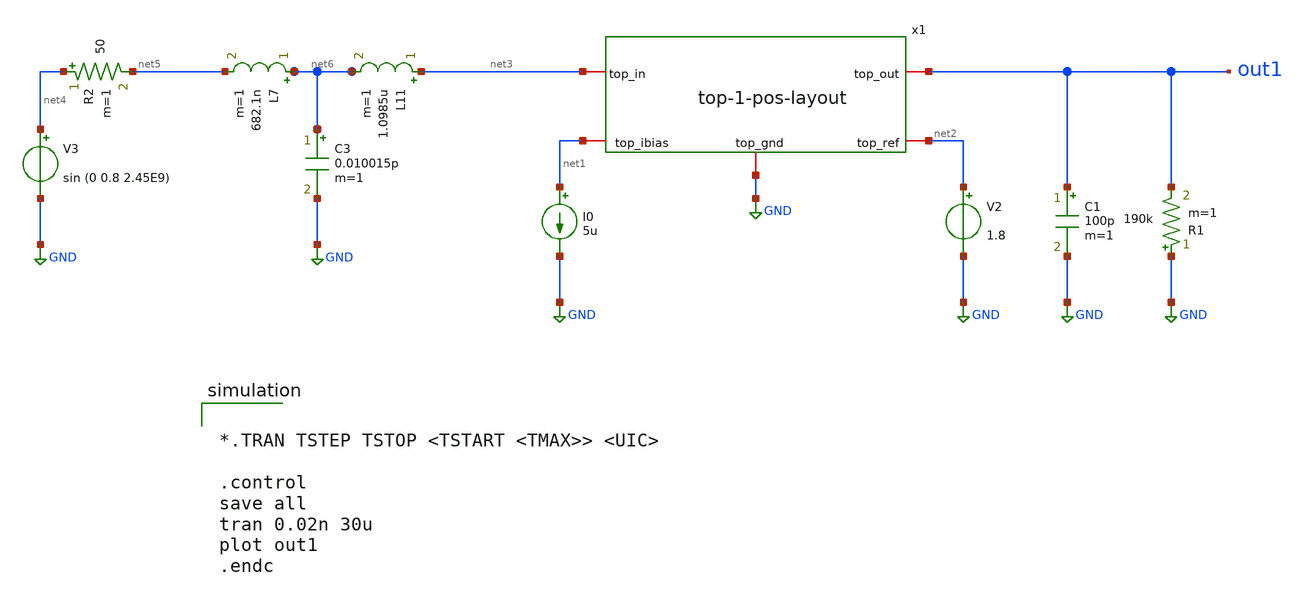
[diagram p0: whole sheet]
** sch_path: xschem/tb-top-1-pos-layout.sch
**.subckt tb-top-1-pos-layout
I0 net1 GND 5u
V2 net2 GND 1.8
C1 out1 GND 100p m=1
R1 GND out1 190k m=1
x1 net3 out1 net2 net1 GND top-1-pos-layout
V3 net4 GND sin (0 0.8 2.45E9)
R2 net4 net5 50 m=1
L7 net6 net5 682.1n m=1
C3 net6 GND 0.010015p m=1
L11 net3 net6 1.0985u m=1
**** begin user architecture code


*.TRAN TSTEP TSTOP <TSTART <TMAX>> <UIC>

.control
save all
tran 0.02n 30u
plot out1
.endc



** opencircuitdesign pdks install
.lib $::SKYWATER_MODELS/sky130.lib.spice tt


**** end user architecture code
**.ends

* expanding   symbol:  top-1-pos-layout.sym # of pins=5
** sym_path: xschem/top-1-pos-layout.sym
** sch_path: xschem/top-1-pos-layout.sch
.subckt top-1-pos-layout top_in top_out top_ref top_ibias top_gnd
*.iopin top_in
*.iopin top_gnd
*.iopin top_ibias
*.iopin top_ref
*.iopin top_out
**** begin user architecture code

* NGSPICE file created from top-1.ext - technology: sky130A

*.subckt top-1 top_ibias top_ref top_out top_in top_gnd
X0 w_13300_10340# top_ibias x1.o x1.o sky130_fd_pr__pfet_g5v0d10v5 ad=5.51e+12p pd=4.206e+07u
+ as=1.392e+13p ps=1.0528e+08u w=3e+06u l=1e+06u
X1 a_11070_13062# x2.x1.Vout sky130_fd_pr__cap_mim_m3_1 l=2.3e+07u w=2.3e+07u
X2 x1.o top_ibias x2.x1.Vout x1.o sky130_fd_pr__pfet_g5v0d10v5 ad=0p pd=0u as=6.09e+12p
+ ps=4.606e+07u w=3e+06u l=1e+06u
X3 x1.o top_ibias w_13300_10340# x1.o sky130_fd_pr__pfet_g5v0d10v5 ad=0p pd=0u as=0p ps=0u w=3e+06u
+ l=1e+06u
X4 x1.o top_ibias w_13300_10340# x1.o sky130_fd_pr__pfet_g5v0d10v5 ad=0p pd=0u as=0p ps=0u w=3e+06u
+ l=1e+06u
X5 top_ibias top_ibias x1.o x1.o sky130_fd_pr__pfet_g5v0d10v5 ad=3.48e+12p pd=2.632e+07u as=0p ps=0u
+ w=3e+06u l=1e+06u
X6 top_out x2.x1.Vout x1.o top_gnd sky130_fd_pr__nfet_03v3_nvt ad=2.9e+12p pd=2.058e+07u
+ as=3.56642e+13p ps=2.4654e+08u w=1e+07u l=500000u
X7 x2.x1.Vout top_ibias x1.o x1.o sky130_fd_pr__pfet_g5v0d10v5 ad=0p pd=0u as=0p ps=0u w=3e+06u
+ l=1e+06u
X8 x2.x1.Vout top_ibias x1.o x1.o sky130_fd_pr__pfet_g5v0d10v5 ad=0p pd=0u as=0p ps=0u w=3e+06u
+ l=1e+06u
X9 w_13300_10340# top_ibias x1.o x1.o sky130_fd_pr__pfet_g5v0d10v5 ad=0p pd=0u as=0p ps=0u w=3e+06u
+ l=1e+06u
X10 x1.o top_ibias top_ibias x1.o sky130_fd_pr__pfet_g5v0d10v5 ad=0p pd=0u as=0p ps=0u w=3e+06u
+ l=1e+06u
X11 x2.x1.Vout top_ibias x1.o x1.o sky130_fd_pr__pfet_g5v0d10v5 ad=0p pd=0u as=0p ps=0u w=3e+06u
+ l=1e+06u
X12 x2.x1.Vout a_11070_13062# top_gnd top_gnd sky130_fd_pr__nfet_g5v0d10v5 ad=3.48e+12p
+ pd=2.632e+07u as=7.54e+12p ps=5.548e+07u w=3e+06u l=1e+06u
X13 x1.o top_ibias x2.x1.Vout x1.o sky130_fd_pr__pfet_g5v0d10v5 ad=0p pd=0u as=0p ps=0u w=3e+06u
+ l=1e+06u
X14 a_11070_13062# top_ref w_13300_10340# w_13300_10340# sky130_fd_pr__pfet_g5v0d10v5 ad=5.8e+11p
+ pd=4.58e+06u as=0p ps=0u w=2e+06u l=500000u
X15 x1.o top_gnd sky130_fd_pr__cap_mim_m3_1 l=3e+07u w=3e+07u
X16 w_100_16400# w_100_16400# top_gnd w_100_16400# sky130_fd_pr__pfet_01v8_lvt ad=1.392e+13p
+ pd=9.948e+07u as=6.96e+12p ps=4.974e+07u w=8e+06u l=350000u
X17 x1.o top_gnd sky130_fd_pr__cap_mim_m3_1 l=3e+07u w=3e+07u
X18 x2.x1.Vout a_11070_13062# top_gnd top_gnd sky130_fd_pr__nfet_g5v0d10v5 ad=0p pd=0u as=0p ps=0u
+ w=3e+06u l=1e+06u
X19 w_100_16400# x1.o x1.o x1.o sky130_fd_pr__pfet_01v8_lvt ad=0p pd=0u as=6.96e+12p ps=4.974e+07u
+ w=8e+06u l=350000u
X20 top_gnd a_11070_13062# x2.x1.Vout top_gnd sky130_fd_pr__nfet_g5v0d10v5 ad=0p pd=0u as=0p ps=0u
+ w=3e+06u l=1e+06u
X21 top_gnd a_11070_13062# x2.x1.Vout top_gnd sky130_fd_pr__nfet_g5v0d10v5 ad=0p pd=0u as=0p ps=0u
+ w=3e+06u l=1e+06u
X22 w_100_16400# x1.o x1.o x1.o sky130_fd_pr__pfet_01v8_lvt ad=0p pd=0u as=0p ps=0u w=8e+06u
+ l=350000u
X23 w_13300_10340# top_ibias x1.o x1.o sky130_fd_pr__pfet_g5v0d10v5 ad=0p pd=0u as=0p ps=0u w=3e+06u
+ l=1e+06u
X24 x1.o top_ibias top_ibias x1.o sky130_fd_pr__pfet_g5v0d10v5 ad=0p pd=0u as=0p ps=0u w=3e+06u
+ l=1e+06u
X25 x1.o top_ibias x2.x1.Vout x1.o sky130_fd_pr__pfet_g5v0d10v5 ad=0p pd=0u as=0p ps=0u w=3e+06u
+ l=1e+06u
X26 top_gnd w_100_16400# w_100_16400# w_100_16400# sky130_fd_pr__pfet_01v8_lvt ad=0p pd=0u as=0p
+ ps=0u w=8e+06u l=350000u
X27 x1.o x1.o w_100_16400# x1.o sky130_fd_pr__pfet_01v8_lvt ad=0p pd=0u as=0p ps=0u w=8e+06u
+ l=350000u
X28 x2.x1.Vout top_ibias x1.o x1.o sky130_fd_pr__pfet_g5v0d10v5 ad=0p pd=0u as=0p ps=0u w=3e+06u
+ l=1e+06u
X29 x1.o top_ibias x2.x1.Vout x1.o sky130_fd_pr__pfet_g5v0d10v5 ad=0p pd=0u as=0p ps=0u w=3e+06u
+ l=1e+06u
X30 top_gnd w_100_16400# w_100_16400# w_100_16400# sky130_fd_pr__pfet_01v8_lvt ad=0p pd=0u as=0p
+ ps=0u w=8e+06u l=350000u
X31 a_13658_10637# top_out w_13300_10340# w_13300_10340# sky130_fd_pr__pfet_g5v0d10v5 ad=5.8e+11p
+ pd=4.58e+06u as=0p ps=0u w=2e+06u l=500000u
X32 top_gnd w_100_16400# w_100_16400# w_100_16400# sky130_fd_pr__pfet_01v8_lvt ad=0p pd=0u as=0p
+ ps=0u w=8e+06u l=350000u
X33 x1.o x1.o w_100_16400# x1.o sky130_fd_pr__pfet_01v8_lvt ad=0p pd=0u as=0p ps=0u w=8e+06u
+ l=350000u
X34 top_ibias top_ibias x1.o x1.o sky130_fd_pr__pfet_g5v0d10v5 ad=0p pd=0u as=0p ps=0u w=3e+06u
+ l=1e+06u
X35 top_gnd a_13658_10637# a_13658_10637# top_gnd sky130_fd_pr__nfet_g5v0d10v5 ad=0p pd=0u
+ as=2.03e+12p ps=1.458e+07u w=7e+06u l=500000u
X36 w_100_16400# top_in sky130_fd_pr__cap_mim_m3_1 l=3e+07u w=3e+07u
X37 top_ibias top_ibias x1.o x1.o sky130_fd_pr__pfet_g5v0d10v5 ad=0p pd=0u as=0p ps=0u w=3e+06u
+ l=1e+06u
X38 x1.o top_ibias top_ibias x1.o sky130_fd_pr__pfet_g5v0d10v5 ad=0p pd=0u as=0p ps=0u w=3e+06u
+ l=1e+06u
X39 top_gnd a_13658_10637# a_11070_13062# top_gnd sky130_fd_pr__nfet_g5v0d10v5 ad=0p pd=0u
+ as=2.03e+12p ps=1.458e+07u w=7e+06u l=500000u
X40 w_100_16400# w_100_16400# top_gnd w_100_16400# sky130_fd_pr__pfet_01v8_lvt ad=0p pd=0u as=0p
+ ps=0u w=8e+06u l=350000u
X41 x1.o top_ibias w_13300_10340# x1.o sky130_fd_pr__pfet_g5v0d10v5 ad=0p pd=0u as=0p ps=0u w=3e+06u
+ l=1e+06u
X42 x2.x1.Vout top_ibias x1.o x1.o sky130_fd_pr__pfet_g5v0d10v5 ad=0p pd=0u as=0p ps=0u w=3e+06u
+ l=1e+06u
X43 x1.o top_ibias x2.x1.Vout x1.o sky130_fd_pr__pfet_g5v0d10v5 ad=0p pd=0u as=0p ps=0u w=3e+06u
+ l=1e+06u
X44 w_13300_10340# top_ibias x1.o x1.o sky130_fd_pr__pfet_g5v0d10v5 ad=0p pd=0u as=0p ps=0u w=3e+06u
+ l=1e+06u
X45 w_100_16400# x1.o x1.o x1.o sky130_fd_pr__pfet_01v8_lvt ad=0p pd=0u as=0p ps=0u w=8e+06u
+ l=350000u
X46 x1.o top_ibias x2.x1.Vout x1.o sky130_fd_pr__pfet_g5v0d10v5 ad=0p pd=0u as=0p ps=0u w=3e+06u
+ l=1e+06u
X47 x1.o top_ibias x2.x1.Vout x1.o sky130_fd_pr__pfet_g5v0d10v5 ad=0p pd=0u as=0p ps=0u w=3e+06u
+ l=1e+06u
X48 x1.o top_gnd sky130_fd_pr__cap_mim_m3_1 l=3e+07u w=3e+07u
X49 top_gnd a_11070_13062# x2.x1.Vout top_gnd sky130_fd_pr__nfet_g5v0d10v5 ad=0p pd=0u as=0p ps=0u
+ w=3e+06u l=1e+06u
X50 top_gnd a_11070_13062# x2.x1.Vout top_gnd sky130_fd_pr__nfet_g5v0d10v5 ad=0p pd=0u as=0p ps=0u
+ w=3e+06u l=1e+06u
X51 top_ibias top_ibias x1.o x1.o sky130_fd_pr__pfet_g5v0d10v5 ad=0p pd=0u as=0p ps=0u w=3e+06u
+ l=1e+06u
X52 x1.o top_ibias top_ibias x1.o sky130_fd_pr__pfet_g5v0d10v5 ad=0p pd=0u as=0p ps=0u w=3e+06u
+ l=1e+06u
X53 x2.x1.Vout a_11070_13062# top_gnd top_gnd sky130_fd_pr__nfet_g5v0d10v5 ad=0p pd=0u as=0p ps=0u
+ w=3e+06u l=1e+06u
X54 x1.o top_ibias w_13300_10340# x1.o sky130_fd_pr__pfet_g5v0d10v5 ad=0p pd=0u as=0p ps=0u w=3e+06u
+ l=1e+06u
X55 x2.x1.Vout top_ibias x1.o x1.o sky130_fd_pr__pfet_g5v0d10v5 ad=0p pd=0u as=0p ps=0u w=3e+06u
+ l=1e+06u
C0 top_ref a_13658_10637# 0.07fF
C1 a_13658_10637# top_ibias 0.05fF
C2 top_ref top_ibias 0.02fF
C3 a_11070_13062# a_13658_10637# 0.13fF
C4 top_ref a_11070_13062# 0.25fF
C5 a_11070_13062# top_ibias 0.62fF
C6 x2.x1.Vout a_13658_10637# 0.01fF
C7 top_out a_13658_10637# 0.35fF
C8 top_ref x2.x1.Vout 0.01fF
C9 top_in x1.o 0.99fF
C10 w_13300_10340# a_13658_10637# 0.58fF
C11 w_100_16400# top_in 77.27fF
C12 a_13658_10637# x1.o 0.07fF
C13 top_ref top_out 0.14fF
C14 w_13300_10340# top_ref 0.35fF
C15 top_ref x1.o 0.08fF
C16 x2.x1.Vout top_ibias 2.47fF
C17 top_out top_ibias 0.06fF
C18 w_13300_10340# top_ibias 2.11fF
C19 x1.o top_ibias 22.39fF
C20 x2.x1.Vout a_11070_13062# 47.08fF
C21 top_out a_11070_13062# 0.32fF
C22 w_13300_10340# a_11070_13062# 0.70fF
C23 a_11070_13062# x1.o 1.57fF
C24 x2.x1.Vout top_out 3.09fF
C25 w_13300_10340# x2.x1.Vout 0.02fF
C26 x2.x1.Vout x1.o 6.10fF
C27 w_13300_10340# top_out 0.59fF
C28 top_out x1.o 0.63fF
C29 w_13300_10340# x1.o 2.69fF
C30 w_100_16400# x1.o 4.45fF
C31 top_in top_gnd 17.62fF
C32 a_13658_10637# top_gnd 2.13fF
C33 top_ref top_gnd 1.38fF
C34 top_ibias top_gnd 5.83fF
C35 a_11070_13062# top_gnd 9.41fF
C36 x2.x1.Vout top_gnd 24.64fF
C37 top_out top_gnd 6.57fF
C38 w_13300_10340# top_gnd 4.41fF
C39 x1.o top_gnd 292.46fF
C40 w_100_16400# top_gnd 15.38fF
*.ends

**** end user architecture code
.ends

.GLOBAL GND
.end
